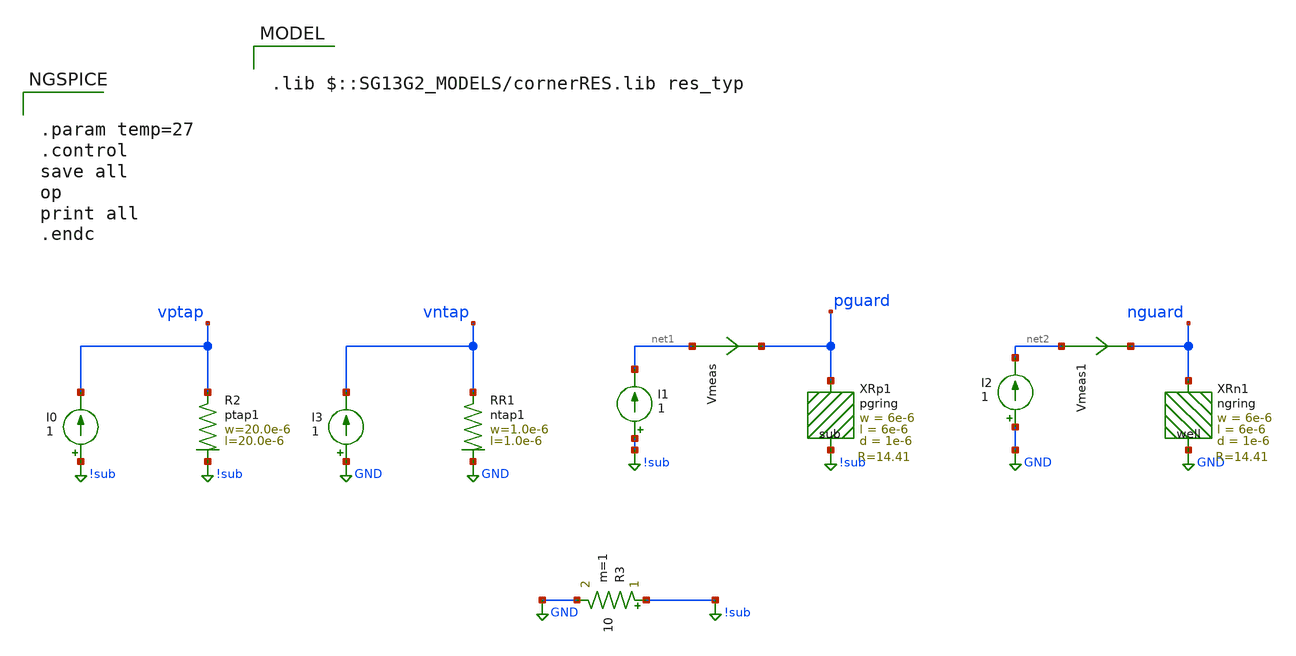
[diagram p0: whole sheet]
** sch_path: ihp-sg13g2/libs.tech/xschem/sg13g2_tests/dc_gring.sch
**.subckt dc_gring
I0 !sub vptap 1
XR2 vptap !sub ptap1 R=2.042 w=20.0e-6 l=20.0e-6
Vmeas net1 pguard 0
.save i(vmeas)
I1 !sub net1 1
Vmeas1 net2 nguard 0
.save i(vmeas1)
I2 GND net2 1
XRp1 pguard !sub pgring R=14.41 w=6e-6 l=6e-6 d=1e-6
XRn1 nguard GND ngring R=14.41 w=6e-6 l=6e-6 d=1e-6
I3 GND vntap 1
XR1 vntap GND ntap1 R=196 w=1.0e-6 l=1.0e-6
R3 !sub GND 10 m=1
**** begin user architecture code


.param temp=27
.control
save all
op
print all
.endc



.lib $::SG13G2_MODELS/cornerRES.lib res_typ

**** end user architecture code
**.ends
.GLOBAL GND
.GLOBAL !sub
.end
